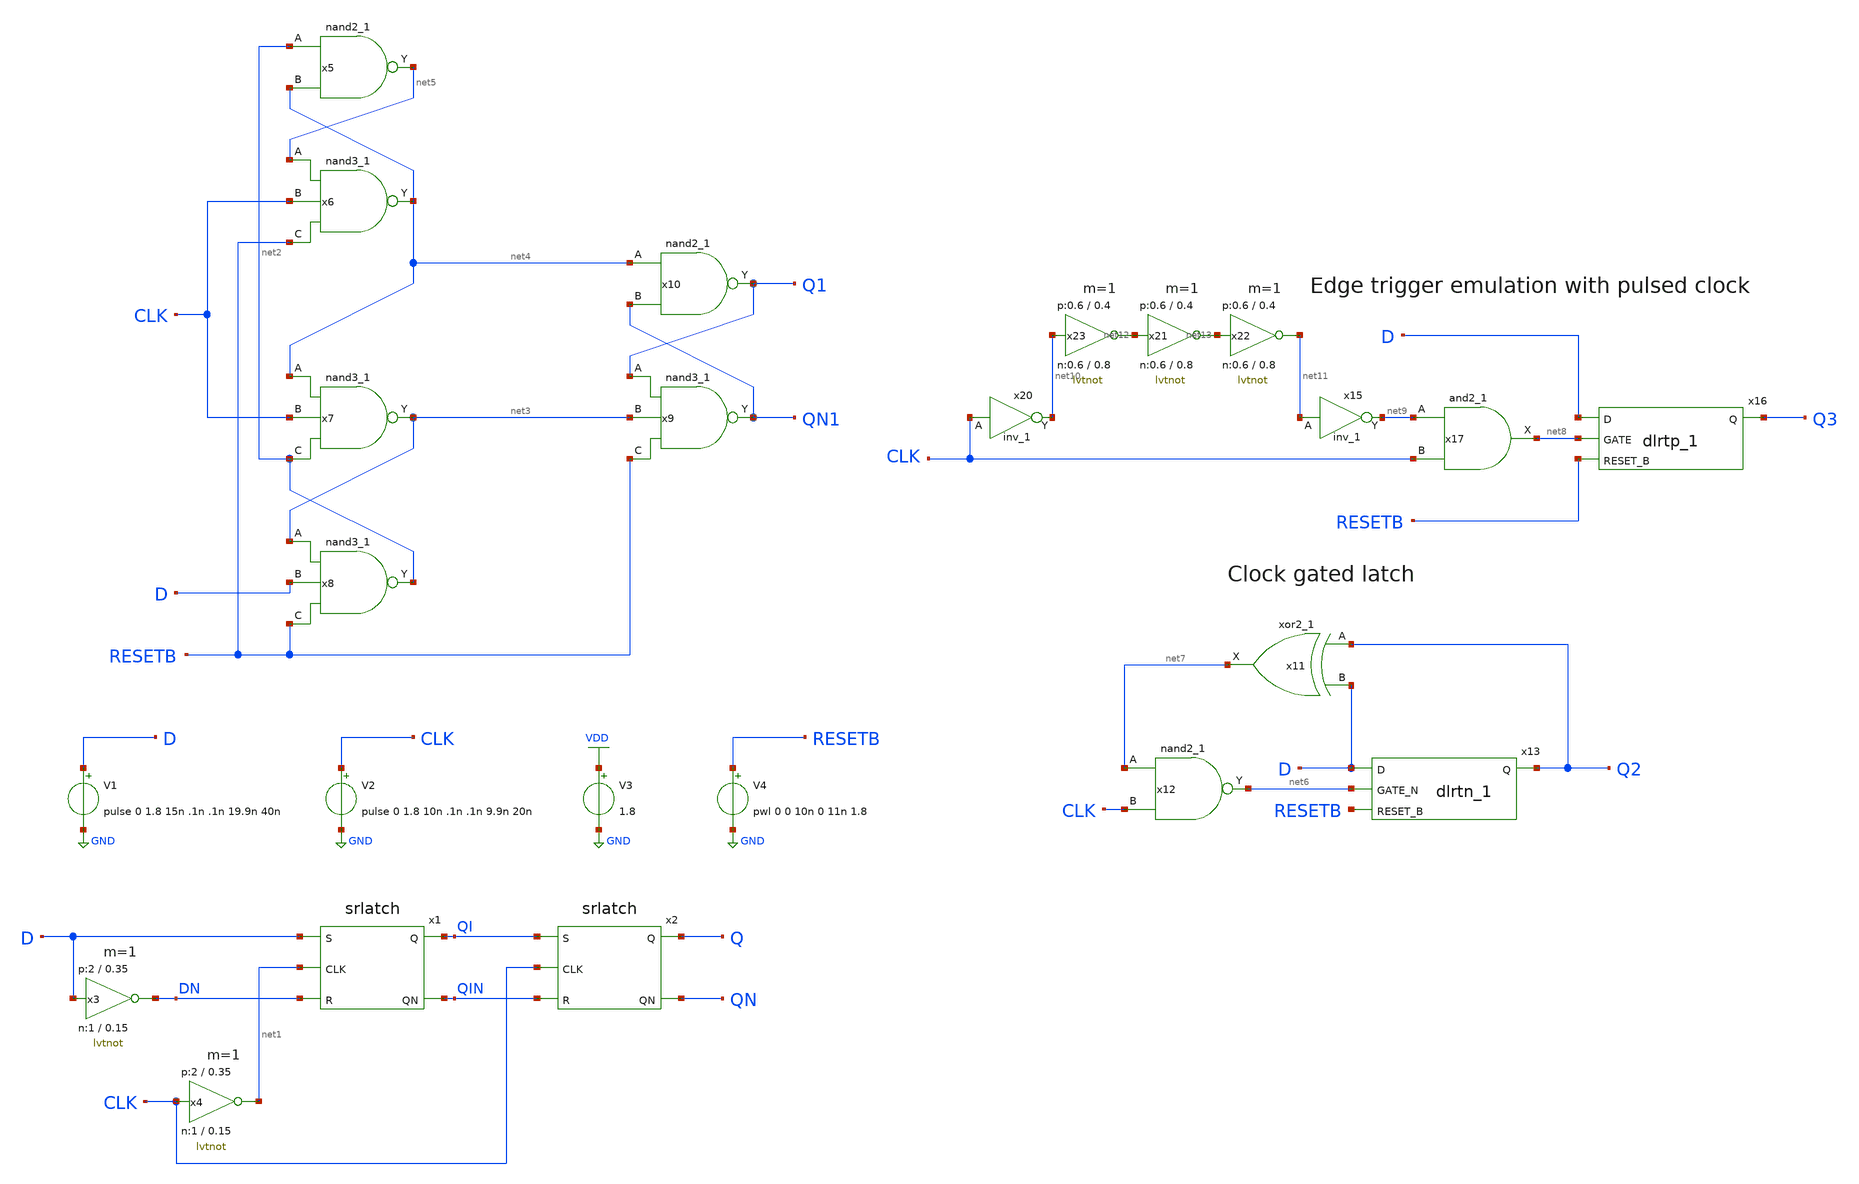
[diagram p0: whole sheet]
** sch_path: sky130_tests/test_ff.sch
* Copyright 2020 Stefan Frederik Schippers
* Licensed under the Apache License, Version 2.0 (the "License");
* you may not use this file except in compliance with the License.
* You may obtain a copy of the License at
* https://www.apache.org/licenses/LICENSE-2.0
* Unless required by applicable law or agreed to in writing, software
* distributed under the License is distributed on an "AS IS" BASIS,
* WITHOUT WARRANTIES OR CONDITIONS OF ANY KIND, either express or implied.
* See the License for the specific language governing permissions and
* limitations under the License.
**.subckt test_ff
x1 D net1 DN QI QIN srlatch
x2 QI CLK QIN Q QN srlatch
x3 D DN VDD GND lvtnot W_N=1 L_N=0.15 W_P=2 L_P=0.35 m=1
x4 CLK net1 VDD GND lvtnot W_N=1 L_N=0.15 W_P=2 L_P=0.35 m=1
V1 D GND pulse 0 1.8 15n .1n .1n 19.9n 40n
V2 CLK GND pulse 0 1.8 10n .1n .1n 9.9n 20n
V3 VDD GND 1.8
x5 net2 net4 GND GND VDD VDD net5 sky130_fd_sc_hd__nand2_1
x6 net5 CLK RESETB GND GND VDD VDD net4 sky130_fd_sc_hd__nand3_1
x7 net4 CLK net2 GND GND VDD VDD net3 sky130_fd_sc_hd__nand3_1
x8 net3 D RESETB GND GND VDD VDD net2 sky130_fd_sc_hd__nand3_1
x9 Q1 net3 RESETB GND GND VDD VDD QN1 sky130_fd_sc_hd__nand3_1
x10 net4 QN1 GND GND VDD VDD Q1 sky130_fd_sc_hd__nand2_1
V4 RESETB GND pwl 0 0 10n 0 11n 1.8
x11 Q2 D GND GND VDD VDD net7 sky130_fd_sc_hd__xor2_1
x13 D net6 RESETB GND GND VDD VDD Q2 sky130_fd_sc_hd__dlrtn_1
x12 net7 CLK GND GND VDD VDD net6 sky130_fd_sc_hd__nand2_1
x15 net11 GND GND VDD VDD net9 sky130_fd_sc_hd__inv_1
x16 D net8 RESETB GND GND VDD VDD Q3 sky130_fd_sc_hd__dlrtp_1
x17 net9 CLK GND GND VDD VDD net8 sky130_fd_sc_hd__and2_1
x20 CLK GND GND VDD VDD net10 sky130_fd_sc_hd__inv_1
x21 net12 net13 VDD GND lvtnot W_N=0.6 L_N=0.8 W_P=0.6 L_P=0.4 m=1
x22 net13 net11 VDD GND lvtnot W_N=0.6 L_N=0.8 W_P=0.6 L_P=0.4 m=1
x23 net10 net12 VDD GND lvtnot W_N=0.6 L_N=0.8 W_P=0.6 L_P=0.4 m=1
**** begin user architecture code

.include $::SKYWATER_MODELS/cells/nfet_01v8/sky130_fd_pr__nfet_01v8__tt.corner.spice
.include $::SKYWATER_MODELS/cells/nfet_01v8_lvt/sky130_fd_pr__nfet_01v8_lvt__tt.corner.spice
.include $::SKYWATER_MODELS/cells/pfet_01v8/sky130_fd_pr__pfet_01v8__tt.corner.spice
.include $::SKYWATER_MODELS/cells/nfet_03v3_nvt/sky130_fd_pr__nfet_03v3_nvt__tt.corner.spice
.include $::SKYWATER_MODELS/cells/nfet_05v0_nvt/sky130_fd_pr__nfet_05v0_nvt__tt.corner.spice
.include $::SKYWATER_MODELS/cells/esd_nfet_01v8/sky130_fd_pr__esd_nfet_01v8__tt.corner.spice
.include $::SKYWATER_MODELS/cells/pfet_01v8_lvt/sky130_fd_pr__pfet_01v8_lvt__tt.corner.spice
.include $::SKYWATER_MODELS/cells/pfet_01v8_hvt/sky130_fd_pr__pfet_01v8_hvt__tt.corner.spice
.include $::SKYWATER_MODELS/cells/esd_pfet_g5v0d10v5/sky130_fd_pr__esd_pfet_g5v0d10v5__tt.corner.spice
.include $::SKYWATER_MODELS/cells/pfet_g5v0d10v5/sky130_fd_pr__pfet_g5v0d10v5__tt.corner.spice
.include $::SKYWATER_MODELS/cells/pfet_g5v0d16v0/sky130_fd_pr__pfet_g5v0d16v0__tt.corner.spice
.include $::SKYWATER_MODELS/cells/nfet_g5v0d10v5/sky130_fd_pr__nfet_g5v0d10v5__tt.corner.spice
.include $::SKYWATER_MODELS/cells/nfet_g5v0d16v0/sky130_fd_pr__nfet_g5v0d16v0__tt_discrete.corner.spice
.include $::SKYWATER_MODELS/cells/esd_nfet_g5v0d10v5/sky130_fd_pr__esd_nfet_g5v0d10v5__tt.corner.spice
.include $::SKYWATER_MODELS/models/corners/tt/nonfet.spice
* Mismatch parameters
.include $::SKYWATER_MODELS/cells/nfet_01v8/sky130_fd_pr__nfet_01v8__mismatch.corner.spice
.include $::SKYWATER_MODELS/cells/pfet_01v8/sky130_fd_pr__pfet_01v8__mismatch.corner.spice
.include $::SKYWATER_MODELS/cells/nfet_01v8_lvt/sky130_fd_pr__nfet_01v8_lvt__mismatch.corner.spice
.include $::SKYWATER_MODELS/cells/pfet_01v8_lvt/sky130_fd_pr__pfet_01v8_lvt__mismatch.corner.spice
.include $::SKYWATER_MODELS/cells/pfet_01v8_hvt/sky130_fd_pr__pfet_01v8_hvt__mismatch.corner.spice
.include $::SKYWATER_MODELS/cells/nfet_g5v0d10v5/sky130_fd_pr__nfet_g5v0d10v5__mismatch.corner.spice
.include $::SKYWATER_MODELS/cells/pfet_g5v0d10v5/sky130_fd_pr__pfet_g5v0d10v5__mismatch.corner.spice
.include $::SKYWATER_MODELS/cells/nfet_05v0_nvt/sky130_fd_pr__nfet_05v0_nvt__mismatch.corner.spice
.include $::SKYWATER_MODELS/cells/nfet_03v3_nvt/sky130_fd_pr__nfet_03v3_nvt__mismatch.corner.spice
* Resistor$::SKYWATER_MODELS/Capacitor
.include $::SKYWATER_MODELS/models/r+c/res_typical__cap_typical.spice
.include $::SKYWATER_MODELS/models/r+c/res_typical__cap_typical__lin.spice
* Special cells
.include $::SKYWATER_MODELS/models/corners/tt/specialized_cells.spice
* All models
.include $::SKYWATER_MODELS/models/all.spice
* Corner
.include $::SKYWATER_MODELS/models/corners/tt/rf.spice

**** end user architecture code
**.ends
.GLOBAL GND
.GLOBAL VDD
**** begin user architecture code



.save all
.options savecurrents
.tran 0.2n 100n


[sky130_models]
**** end user architecture code
.end
